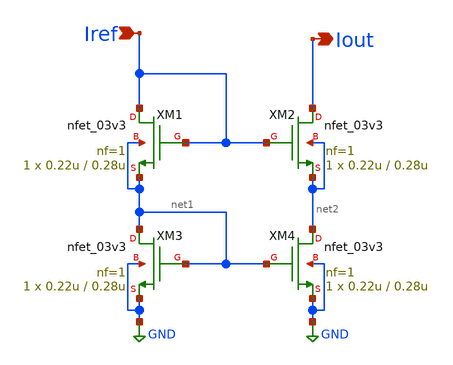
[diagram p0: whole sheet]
** sch_path: designs/libs/core_analog/current-mirror/nmos_current_mirror.sch
**.subckt nmos_current_mirror Iref Iout
*.ipin Iref
*.opin Iout
XM1 Iref Iref net1 net1 nfet_03v3 L=0.28u W=0.22u nf=1 ad='int((nf+1)/2) * W/nf * 0.18u' as='int((nf+2)/2) * W/nf * 0.18u'
+ pd='2*int((nf+1)/2) * (W/nf + 0.18u)' ps='2*int((nf+2)/2) * (W/nf + 0.18u)' nrd='0.18u / W' nrs='0.18u / W'
+ sa=0 sb=0 sd=0 m=1
XM2 Iout Iref net2 net2 nfet_03v3 L=0.28u W=0.22u nf=1 ad='int((nf+1)/2) * W/nf * 0.18u' as='int((nf+2)/2) * W/nf * 0.18u'
+ pd='2*int((nf+1)/2) * (W/nf + 0.18u)' ps='2*int((nf+2)/2) * (W/nf + 0.18u)' nrd='0.18u / W' nrs='0.18u / W'
+ sa=0 sb=0 sd=0 m=1
XM3 net1 net1 GND GND nfet_03v3 L=0.28u W=0.22u nf=1 ad='int((nf+1)/2) * W/nf * 0.18u' as='int((nf+2)/2) * W/nf * 0.18u'
+ pd='2*int((nf+1)/2) * (W/nf + 0.18u)' ps='2*int((nf+2)/2) * (W/nf + 0.18u)' nrd='0.18u / W' nrs='0.18u / W'
+ sa=0 sb=0 sd=0 m=1
XM4 net2 net1 GND GND nfet_03v3 L=0.28u W=0.22u nf=1 ad='int((nf+1)/2) * W/nf * 0.18u' as='int((nf+2)/2) * W/nf * 0.18u'
+ pd='2*int((nf+1)/2) * (W/nf + 0.18u)' ps='2*int((nf+2)/2) * (W/nf + 0.18u)' nrd='0.18u / W' nrs='0.18u / W'
+ sa=0 sb=0 sd=0 m=1
**.ends
.GLOBAL GND
.end
